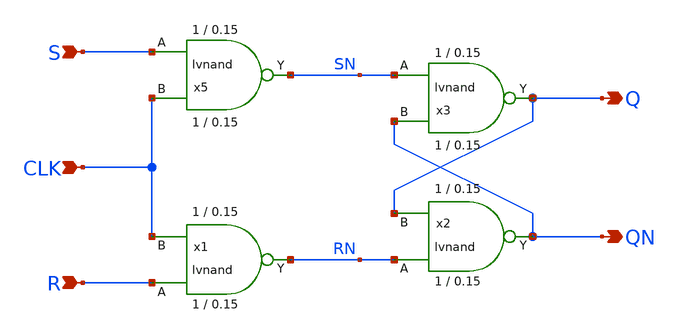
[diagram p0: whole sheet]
** sch_path: xyce/sky130A-xyce/libs.tech/xschem/sky130_tests/srlatch.sch
* Copyright 2020 Stefan Frederik Schippers
* Licensed under the Apache License, Version 2.0 (the "License");
* you may not use this file except in compliance with the License.
* You may obtain a copy of the License at
* https://www.apache.org/licenses/LICENSE-2.0
* Unless required by applicable law or agreed to in writing, software
* distributed under the License is distributed on an "AS IS" BASIS,
* WITHOUT WARRANTIES OR CONDITIONS OF ANY KIND, either express or implied.
* See the License for the specific language governing permissions and
* limitations under the License.
**.subckt srlatch S R Q QN CLK
*.ipin S
*.ipin R
*.opin Q
*.opin QN
*.ipin CLK
x5 S CLK SN VCC VSS lvnand WidthN=1 LenN=0.15 WidthP=1 LenP=0.15 m=1
x1 R CLK RN VCC VSS lvnand WidthN=1 LenN=0.15 WidthP=1 LenP=0.15 m=1
x2 RN Q QN VCC VSS lvnand WidthN=1 LenN=0.15 WidthP=1 LenP=0.15 m=1
x3 SN QN Q VCC VSS lvnand WidthN=1 LenN=0.15 WidthP=1 LenP=0.15 m=1
**** begin user architecture code

.include $::SKYWATER_MODELS/cells/nfet_01v8/sky130_fd_pr__nfet_01v8__tt.corner.spice
.include $::SKYWATER_MODELS/cells/nfet_01v8_lvt/sky130_fd_pr__nfet_01v8_lvt__tt.corner.spice
.include $::SKYWATER_MODELS/cells/pfet_01v8/sky130_fd_pr__pfet_01v8__tt.corner.spice
.include $::SKYWATER_MODELS/cells/nfet_03v3_nvt/sky130_fd_pr__nfet_03v3_nvt__tt.corner.spice
.include $::SKYWATER_MODELS/cells/nfet_05v0_nvt/sky130_fd_pr__nfet_05v0_nvt__tt.corner.spice
.include $::SKYWATER_MODELS/cells/esd_nfet_01v8/sky130_fd_pr__esd_nfet_01v8__tt.corner.spice
.include $::SKYWATER_MODELS/cells/pfet_01v8_lvt/sky130_fd_pr__pfet_01v8_lvt__tt.corner.spice
.include $::SKYWATER_MODELS/cells/pfet_01v8_hvt/sky130_fd_pr__pfet_01v8_hvt__tt.corner.spice
.include $::SKYWATER_MODELS/cells/esd_pfet_g5v0d10v5/sky130_fd_pr__esd_pfet_g5v0d10v5__tt.corner.spice
.include $::SKYWATER_MODELS/cells/pfet_g5v0d10v5/sky130_fd_pr__pfet_g5v0d10v5__tt.corner.spice
.include $::SKYWATER_MODELS/cells/pfet_g5v0d16v0/sky130_fd_pr__pfet_g5v0d16v0__tt.corner.spice
.include $::SKYWATER_MODELS/cells/nfet_g5v0d10v5/sky130_fd_pr__nfet_g5v0d10v5__tt.corner.spice
.include $::SKYWATER_MODELS/cells/nfet_g5v0d16v0/sky130_fd_pr__nfet_g5v0d16v0__tt_discrete.corner.spice
.include $::SKYWATER_MODELS/cells/esd_nfet_g5v0d10v5/sky130_fd_pr__esd_nfet_g5v0d10v5__tt.corner.spice
.include $::SKYWATER_MODELS/models/corners/tt/nonfet.spice
* Mismatch parameters
.include $::SKYWATER_MODELS/cells/nfet_01v8/sky130_fd_pr__nfet_01v8__mismatch.corner.spice
.include $::SKYWATER_MODELS/cells/pfet_01v8/sky130_fd_pr__pfet_01v8__mismatch.corner.spice
.include $::SKYWATER_MODELS/cells/nfet_01v8_lvt/sky130_fd_pr__nfet_01v8_lvt__mismatch.corner.spice
.include $::SKYWATER_MODELS/cells/pfet_01v8_lvt/sky130_fd_pr__pfet_01v8_lvt__mismatch.corner.spice
.include $::SKYWATER_MODELS/cells/pfet_01v8_hvt/sky130_fd_pr__pfet_01v8_hvt__mismatch.corner.spice
.include $::SKYWATER_MODELS/cells/nfet_g5v0d10v5/sky130_fd_pr__nfet_g5v0d10v5__mismatch.corner.spice
.include $::SKYWATER_MODELS/cells/pfet_g5v0d10v5/sky130_fd_pr__pfet_g5v0d10v5__mismatch.corner.spice
.include $::SKYWATER_MODELS/cells/nfet_05v0_nvt/sky130_fd_pr__nfet_05v0_nvt__mismatch.corner.spice
.include $::SKYWATER_MODELS/cells/nfet_03v3_nvt/sky130_fd_pr__nfet_03v3_nvt__mismatch.corner.spice
* Resistor$::SKYWATER_MODELS/Capacitor
.include $::SKYWATER_MODELS/models/r+c/res_typical__cap_typical.spice
.include $::SKYWATER_MODELS/models/r+c/res_typical__cap_typical__lin.spice
* Special cells
.include $::SKYWATER_MODELS/models/corners/tt/specialized_cells.spice
* All models
.include $::SKYWATER_MODELS/models/all.spice
* Corner
.include $::SKYWATER_MODELS/models/corners/tt/rf.spice

**** end user architecture code
**.ends

* expanding   symbol:  sky130_tests/lvnand.sym # of pins=3
** sym_path: xyce/sky130A-xyce/libs.tech/xschem/sky130_tests/lvnand.sym
** sch_path: xyce/sky130A-xyce/libs.tech/xschem/sky130_tests/lvnand.sch
.subckt lvnand A B Y VCCPIN VSSPIN  WidthN=1 LenN=0.15 WidthP=1 LenP=0.15
*.ipin A
*.ipin B
*.opin Y
XM1 Y B S VSSPIN sky130_fd_pr__nfet_01v8 L=LenN W=WidthN nf=1 ad='int((nf+1)/2) * W/nf * 0.29' as='int((nf+2)/2) * W/nf * 0.29'
+ pd='2*int((nf+1)/2) * (W/nf + 0.29)' ps='2*int((nf+2)/2) * (W/nf + 0.29)' nrd='0.29 / W' nrs='0.29 / W'
+ sa=0 sb=0 sd=0 mult=1 m=1
XM2 Y A VCCPIN VCCPIN sky130_fd_pr__pfet_01v8 L=LenP W=WidthP nf=1 ad='int((nf+1)/2) * W/nf * 0.29' as='int((nf+2)/2) * W/nf * 0.29'
+ pd='2*int((nf+1)/2) * (W/nf + 0.29)' ps='2*int((nf+2)/2) * (W/nf + 0.29)' nrd='0.29 / W' nrs='0.29 / W'
+ sa=0 sb=0 sd=0 mult=1 m=1
XM3 Y B VCCPIN VCCPIN sky130_fd_pr__pfet_01v8 L=LenP W=WidthP nf=1 ad='int((nf+1)/2) * W/nf * 0.29' as='int((nf+2)/2) * W/nf * 0.29'
+ pd='2*int((nf+1)/2) * (W/nf + 0.29)' ps='2*int((nf+2)/2) * (W/nf + 0.29)' nrd='0.29 / W' nrs='0.29 / W'
+ sa=0 sb=0 sd=0 mult=1 m=1
XM4 S A VSSPIN VSSPIN sky130_fd_pr__nfet_01v8 L=LenN W=WidthN nf=1 ad='int((nf+1)/2) * W/nf * 0.29' as='int((nf+2)/2) * W/nf * 0.29'
+ pd='2*int((nf+1)/2) * (W/nf + 0.29)' ps='2*int((nf+2)/2) * (W/nf + 0.29)' nrd='0.29 / W' nrs='0.29 / W'
+ sa=0 sb=0 sd=0 mult=1 m=1
.ends

**** begin user architecture code

* .option SCALE=1e-6
.option method=gear seed=12
.param L=0.15
.param W=0.5

vd d 0 0
vg g 0 0
.control
dc vd 0 2 0.01 vg 0 2 0.2
alterparam L=0.18
alterparam W=1
reset
dc vd 0 2 0.01 vg 0 2 0.2
alterparam L=0.3
alterparam W=2
reset
dc vd 0 2 0.01 vg 0 2 0.2
alterparam L=0.5
alterparam W=3
reset
dc vd 0 2 0.01 vg 0 2 0.2

.endc





**** end user architecture code
.end
